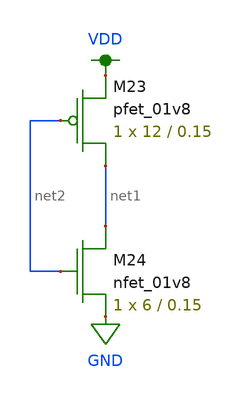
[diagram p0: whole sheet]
** sch_path: schematic/inverter_large.sch
**.subckt inverter_large
XM23 net1 net2 VDD VDD sky130_fd_pr__pfet_01v8 L=0.15 W=12 nf=1 ad='int((nf+1)/2) * W/nf * 0.29' as='int((nf+2)/2) * W/nf * 0.29'
+ pd='2*int((nf+1)/2) * (W/nf + 0.29)' ps='2*int((nf+2)/2) * (W/nf + 0.29)' nrd='0.29 / W' nrs='0.29 / W'
+ sa=0 sb=0 sd=0 mult=1 m=1
XM24 net1 net2 GND GND sky130_fd_pr__nfet_01v8 L=0.15 W=6 nf=1 ad='int((nf+1)/2) * W/nf * 0.29' as='int((nf+2)/2) * W/nf * 0.29'
+ pd='2*int((nf+1)/2) * (W/nf + 0.29)' ps='2*int((nf+2)/2) * (W/nf + 0.29)' nrd='0.29 / W' nrs='0.29 / W'
+ sa=0 sb=0 sd=0 mult=1 m=1
**.ends
.GLOBAL VDD
.GLOBAL GND
.end
